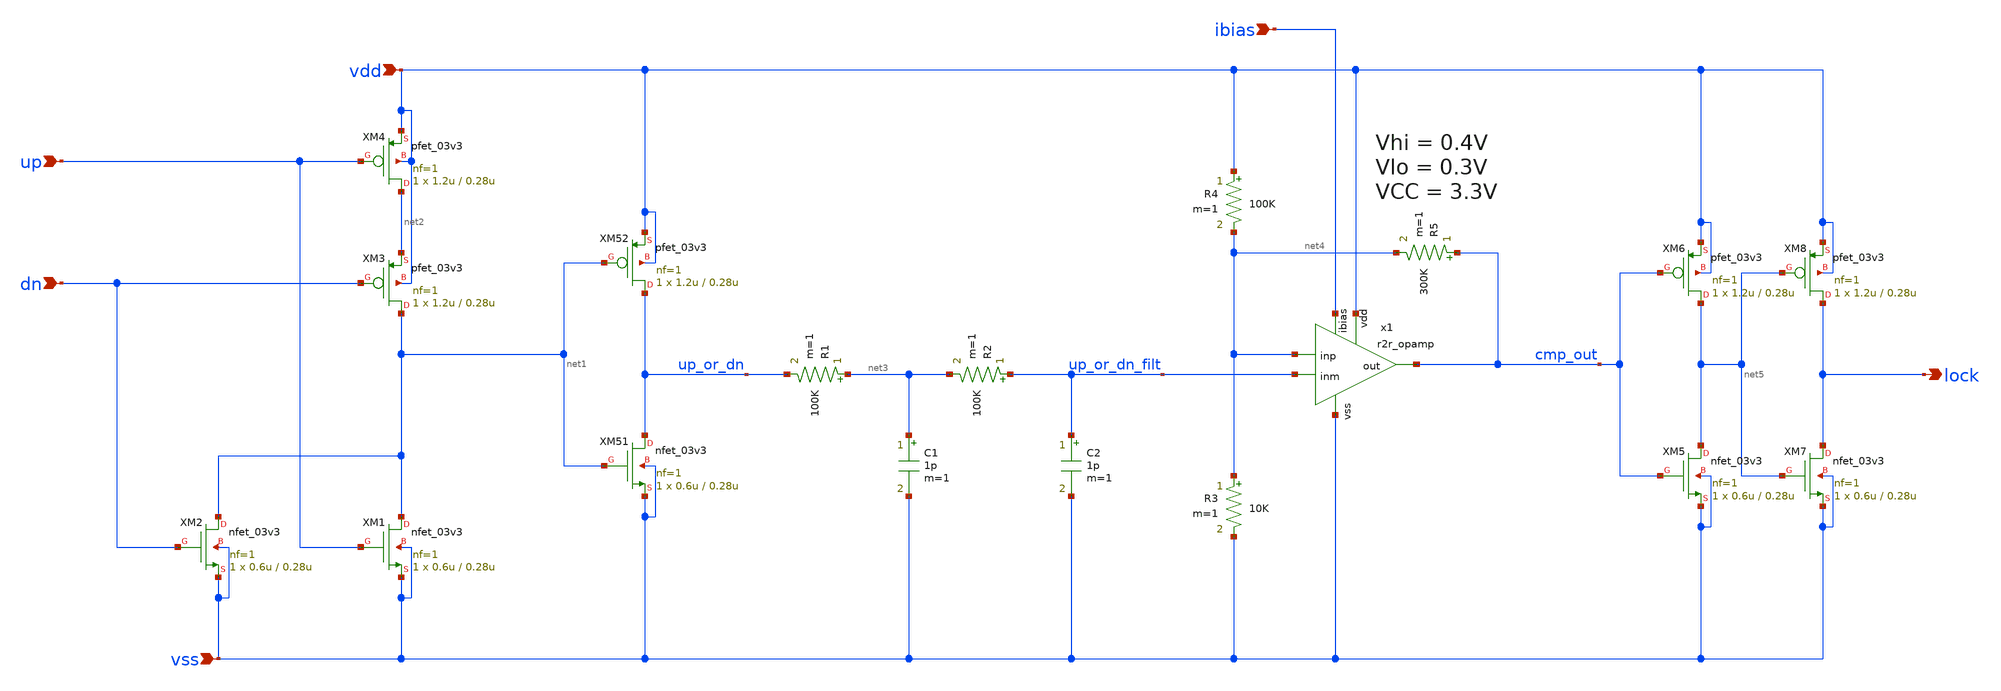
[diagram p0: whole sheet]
** sch_path: xschem/lock_detector.sch
**.subckt lock_detector up dn vdd vss ibias lock
*.ipin up
*.ipin dn
*.ipin vdd
*.ipin vss
*.ipin ibias
*.opin lock
XM51 up_or_dn net1 vss vss nfet_03v3 L=0.28u W=0.6u nf=1 ad='int((nf+1)/2) * W/nf * 0.18u' as='int((nf+2)/2) * W/nf * 0.18u'
+ pd='2*int((nf+1)/2) * (W/nf + 0.18u)' ps='2*int((nf+2)/2) * (W/nf + 0.18u)' nrd='0.18u / W' nrs='0.18u / W'
+ sa=0 sb=0 sd=0 m=1
XM52 up_or_dn net1 vdd vdd pfet_03v3 L=0.28u W=1.2u nf=1 ad='int((nf+1)/2) * W/nf * 0.18u' as='int((nf+2)/2) * W/nf * 0.18u'
+ pd='2*int((nf+1)/2) * (W/nf + 0.18u)' ps='2*int((nf+2)/2) * (W/nf + 0.18u)' nrd='0.18u / W' nrs='0.18u / W'
+ sa=0 sb=0 sd=0 m=1
XM1 net1 up vss vss nfet_03v3 L=0.28u W=0.6u nf=1 ad='int((nf+1)/2) * W/nf * 0.18u' as='int((nf+2)/2) * W/nf * 0.18u'
+ pd='2*int((nf+1)/2) * (W/nf + 0.18u)' ps='2*int((nf+2)/2) * (W/nf + 0.18u)' nrd='0.18u / W' nrs='0.18u / W'
+ sa=0 sb=0 sd=0 m=1
XM2 net1 dn vss vss nfet_03v3 L=0.28u W=0.6u nf=1 ad='int((nf+1)/2) * W/nf * 0.18u' as='int((nf+2)/2) * W/nf * 0.18u'
+ pd='2*int((nf+1)/2) * (W/nf + 0.18u)' ps='2*int((nf+2)/2) * (W/nf + 0.18u)' nrd='0.18u / W' nrs='0.18u / W'
+ sa=0 sb=0 sd=0 m=1
XM3 net1 dn net2 vdd pfet_03v3 L=0.28u W=1.2u nf=1 ad='int((nf+1)/2) * W/nf * 0.18u' as='int((nf+2)/2) * W/nf * 0.18u'
+ pd='2*int((nf+1)/2) * (W/nf + 0.18u)' ps='2*int((nf+2)/2) * (W/nf + 0.18u)' nrd='0.18u / W' nrs='0.18u / W'
+ sa=0 sb=0 sd=0 m=1
XM4 net2 up vdd vdd pfet_03v3 L=0.28u W=1.2u nf=1 ad='int((nf+1)/2) * W/nf * 0.18u' as='int((nf+2)/2) * W/nf * 0.18u'
+ pd='2*int((nf+1)/2) * (W/nf + 0.18u)' ps='2*int((nf+2)/2) * (W/nf + 0.18u)' nrd='0.18u / W' nrs='0.18u / W'
+ sa=0 sb=0 sd=0 m=1
R1 net3 up_or_dn 100K m=1
C1 net3 vss 1p m=1
R2 up_or_dn_filt net3 100K m=1
C2 up_or_dn_filt vss 1p m=1
x1 vdd cmp_out ibias net4 up_or_dn_filt vss r2r_opamp
R3 net4 vss 10K m=1
R4 vdd net4 100K m=1
R5 cmp_out net4 300K m=1
XM5 net5 cmp_out vss vss nfet_03v3 L=0.28u W=0.6u nf=1 ad='int((nf+1)/2) * W/nf * 0.18u' as='int((nf+2)/2) * W/nf * 0.18u'
+ pd='2*int((nf+1)/2) * (W/nf + 0.18u)' ps='2*int((nf+2)/2) * (W/nf + 0.18u)' nrd='0.18u / W' nrs='0.18u / W'
+ sa=0 sb=0 sd=0 m=1
XM6 net5 cmp_out vdd vdd pfet_03v3 L=0.28u W=1.2u nf=1 ad='int((nf+1)/2) * W/nf * 0.18u' as='int((nf+2)/2) * W/nf * 0.18u'
+ pd='2*int((nf+1)/2) * (W/nf + 0.18u)' ps='2*int((nf+2)/2) * (W/nf + 0.18u)' nrd='0.18u / W' nrs='0.18u / W'
+ sa=0 sb=0 sd=0 m=1
XM7 lock net5 vss vss nfet_03v3 L=0.28u W=0.6u nf=1 ad='int((nf+1)/2) * W/nf * 0.18u' as='int((nf+2)/2) * W/nf * 0.18u'
+ pd='2*int((nf+1)/2) * (W/nf + 0.18u)' ps='2*int((nf+2)/2) * (W/nf + 0.18u)' nrd='0.18u / W' nrs='0.18u / W'
+ sa=0 sb=0 sd=0 m=1
XM8 lock net5 vdd vdd pfet_03v3 L=0.28u W=1.2u nf=1 ad='int((nf+1)/2) * W/nf * 0.18u' as='int((nf+2)/2) * W/nf * 0.18u'
+ pd='2*int((nf+1)/2) * (W/nf + 0.18u)' ps='2*int((nf+2)/2) * (W/nf + 0.18u)' nrd='0.18u / W' nrs='0.18u / W'
+ sa=0 sb=0 sd=0 m=1
**.ends

* expanding   symbol:  r2r_opamp.sym # of pins=6
** sym_path: xschem/r2r_opamp.sym
** sch_path: xschem/r2r_opamp.sch
.subckt r2r_opamp vdd out ibias inp inm vss
*.ipin vss
*.ipin vdd
*.ipin ibias
*.ipin inp
*.ipin inm
*.opin out
XM1 net3 inp net8 vss nfet_03v3 L=0.28u W=16u nf=1 ad='int((nf+1)/2) * W/nf * 0.18u' as='int((nf+2)/2) * W/nf * 0.18u'
+ pd='2*int((nf+1)/2) * (W/nf + 0.18u)' ps='2*int((nf+2)/2) * (W/nf + 0.18u)' nrd='0.18u / W' nrs='0.18u / W'
+ sa=0 sb=0 sd=0 m=1
XM2 net4 inm net8 vss nfet_03v3 L=0.28u W=16u nf=1 ad='int((nf+1)/2) * W/nf * 0.18u' as='int((nf+2)/2) * W/nf * 0.18u'
+ pd='2*int((nf+1)/2) * (W/nf + 0.18u)' ps='2*int((nf+2)/2) * (W/nf + 0.18u)' nrd='0.18u / W' nrs='0.18u / W'
+ sa=0 sb=0 sd=0 m=1
XM3 net8 ibias vss vss nfet_03v3 L=0.5u W=16u nf=1 ad='int((nf+1)/2) * W/nf * 0.18u' as='int((nf+2)/2) * W/nf * 0.18u'
+ pd='2*int((nf+1)/2) * (W/nf + 0.18u)' ps='2*int((nf+2)/2) * (W/nf + 0.18u)' nrd='0.18u / W' nrs='0.18u / W'
+ sa=0 sb=0 sd=0 m=1
XM4 net6 inp net1 vdd pfet_03v3 L=0.28u W=32u nf=1 ad='int((nf+1)/2) * W/nf * 0.18u' as='int((nf+2)/2) * W/nf * 0.18u'
+ pd='2*int((nf+1)/2) * (W/nf + 0.18u)' ps='2*int((nf+2)/2) * (W/nf + 0.18u)' nrd='0.18u / W' nrs='0.18u / W'
+ sa=0 sb=0 sd=0 m=1
XM5 net7 inm net1 vdd pfet_03v3 L=0.28u W=32u nf=1 ad='int((nf+1)/2) * W/nf * 0.18u' as='int((nf+2)/2) * W/nf * 0.18u'
+ pd='2*int((nf+1)/2) * (W/nf + 0.18u)' ps='2*int((nf+2)/2) * (W/nf + 0.18u)' nrd='0.18u / W' nrs='0.18u / W'
+ sa=0 sb=0 sd=0 m=1
XM6 net1 net2 vdd vdd pfet_03v3 L=0.5u W=32u nf=1 ad='int((nf+1)/2) * W/nf * 0.18u' as='int((nf+2)/2) * W/nf * 0.18u'
+ pd='2*int((nf+1)/2) * (W/nf + 0.18u)' ps='2*int((nf+2)/2) * (W/nf + 0.18u)' nrd='0.18u / W' nrs='0.18u / W'
+ sa=0 sb=0 sd=0 m=1
XM7 net5 vbiasn net6 vss nfet_03v3 L=0.5u W=8u nf=1 ad='int((nf+1)/2) * W/nf * 0.18u' as='int((nf+2)/2) * W/nf * 0.18u'
+ pd='2*int((nf+1)/2) * (W/nf + 0.18u)' ps='2*int((nf+2)/2) * (W/nf + 0.18u)' nrd='0.18u / W' nrs='0.18u / W'
+ sa=0 sb=0 sd=0 m=1
XM8 out vbiasn net7 vss nfet_03v3 L=0.5u W=8u nf=1 ad='int((nf+1)/2) * W/nf * 0.18u' as='int((nf+2)/2) * W/nf * 0.18u'
+ pd='2*int((nf+1)/2) * (W/nf + 0.18u)' ps='2*int((nf+2)/2) * (W/nf + 0.18u)' nrd='0.18u / W' nrs='0.18u / W'
+ sa=0 sb=0 sd=0 m=1
XM9 net6 ibias vss vss nfet_03v3 L=0.5u W=16u nf=1 ad='int((nf+1)/2) * W/nf * 0.18u' as='int((nf+2)/2) * W/nf * 0.18u'
+ pd='2*int((nf+1)/2) * (W/nf + 0.18u)' ps='2*int((nf+2)/2) * (W/nf + 0.18u)' nrd='0.18u / W' nrs='0.18u / W'
+ sa=0 sb=0 sd=0 m=1
XM10 net7 ibias vss vss nfet_03v3 L=0.5u W=16u nf=1 ad='int((nf+1)/2) * W/nf * 0.18u' as='int((nf+2)/2) * W/nf * 0.18u'
+ pd='2*int((nf+1)/2) * (W/nf + 0.18u)' ps='2*int((nf+2)/2) * (W/nf + 0.18u)' nrd='0.18u / W' nrs='0.18u / W'
+ sa=0 sb=0 sd=0 m=1
XM11 net5 vbiasp net3 vdd pfet_03v3 L=0.5u W=16u nf=1 ad='int((nf+1)/2) * W/nf * 0.18u' as='int((nf+2)/2) * W/nf * 0.18u'
+ pd='2*int((nf+1)/2) * (W/nf + 0.18u)' ps='2*int((nf+2)/2) * (W/nf + 0.18u)' nrd='0.18u / W' nrs='0.18u / W'
+ sa=0 sb=0 sd=0 m=1
XM12 out vbiasp net4 vdd pfet_03v3 L=0.5u W=16u nf=1 ad='int((nf+1)/2) * W/nf * 0.18u' as='int((nf+2)/2) * W/nf * 0.18u'
+ pd='2*int((nf+1)/2) * (W/nf + 0.18u)' ps='2*int((nf+2)/2) * (W/nf + 0.18u)' nrd='0.18u / W' nrs='0.18u / W'
+ sa=0 sb=0 sd=0 m=1
XM13 net3 net5 vdd vdd pfet_03v3 L=0.5u W=32u nf=1 ad='int((nf+1)/2) * W/nf * 0.18u' as='int((nf+2)/2) * W/nf * 0.18u'
+ pd='2*int((nf+1)/2) * (W/nf + 0.18u)' ps='2*int((nf+2)/2) * (W/nf + 0.18u)' nrd='0.18u / W' nrs='0.18u / W'
+ sa=0 sb=0 sd=0 m=1
XM14 net4 net5 vdd vdd pfet_03v3 L=0.5u W=32u nf=1 ad='int((nf+1)/2) * W/nf * 0.18u' as='int((nf+2)/2) * W/nf * 0.18u'
+ pd='2*int((nf+1)/2) * (W/nf + 0.18u)' ps='2*int((nf+2)/2) * (W/nf + 0.18u)' nrd='0.18u / W' nrs='0.18u / W'
+ sa=0 sb=0 sd=0 m=1
XM15 ibias ibias vss vss nfet_03v3 L=0.5u W=2u nf=1 ad='int((nf+1)/2) * W/nf * 0.18u' as='int((nf+2)/2) * W/nf * 0.18u'
+ pd='2*int((nf+1)/2) * (W/nf + 0.18u)' ps='2*int((nf+2)/2) * (W/nf + 0.18u)' nrd='0.18u / W' nrs='0.18u / W'
+ sa=0 sb=0 sd=0 m=1
XM16 net2 ibias vss vss nfet_03v3 L=0.5u W=2u nf=1 ad='int((nf+1)/2) * W/nf * 0.18u' as='int((nf+2)/2) * W/nf * 0.18u'
+ pd='2*int((nf+1)/2) * (W/nf + 0.18u)' ps='2*int((nf+2)/2) * (W/nf + 0.18u)' nrd='0.18u / W' nrs='0.18u / W'
+ sa=0 sb=0 sd=0 m=1
XM17 net2 net2 vdd vdd pfet_03v3 L=0.5u W=4u nf=1 ad='int((nf+1)/2) * W/nf * 0.18u' as='int((nf+2)/2) * W/nf * 0.18u'
+ pd='2*int((nf+1)/2) * (W/nf + 0.18u)' ps='2*int((nf+2)/2) * (W/nf + 0.18u)' nrd='0.18u / W' nrs='0.18u / W'
+ sa=0 sb=0 sd=0 m=1
XM18 vbiasp ibias vss vss nfet_03v3 L=0.5u W=8u nf=1 ad='int((nf+1)/2) * W/nf * 0.18u' as='int((nf+2)/2) * W/nf * 0.18u'
+ pd='2*int((nf+1)/2) * (W/nf + 0.18u)' ps='2*int((nf+2)/2) * (W/nf + 0.18u)' nrd='0.18u / W' nrs='0.18u / W'
+ sa=0 sb=0 sd=0 m=1
XM19 vbiasp vbiasp vdd vdd pfet_03v3 L=0.5u W=4u nf=1 ad='int((nf+1)/2) * W/nf * 0.18u' as='int((nf+2)/2) * W/nf * 0.18u'
+ pd='2*int((nf+1)/2) * (W/nf + 0.18u)' ps='2*int((nf+2)/2) * (W/nf + 0.18u)' nrd='0.18u / W' nrs='0.18u / W'
+ sa=0 sb=0 sd=0 m=1
XM20 vbiasn net2 vdd vdd pfet_03v3 L=0.5u W=16u nf=1 ad='int((nf+1)/2) * W/nf * 0.18u' as='int((nf+2)/2) * W/nf * 0.18u'
+ pd='2*int((nf+1)/2) * (W/nf + 0.18u)' ps='2*int((nf+2)/2) * (W/nf + 0.18u)' nrd='0.18u / W' nrs='0.18u / W'
+ sa=0 sb=0 sd=0 m=1
XM21 vbiasn vbiasn vss vss nfet_03v3 L=0.5u W=2u nf=1 ad='int((nf+1)/2) * W/nf * 0.18u' as='int((nf+2)/2) * W/nf * 0.18u'
+ pd='2*int((nf+1)/2) * (W/nf + 0.18u)' ps='2*int((nf+2)/2) * (W/nf + 0.18u)' nrd='0.18u / W' nrs='0.18u / W'
+ sa=0 sb=0 sd=0 m=1
.ends

.end
